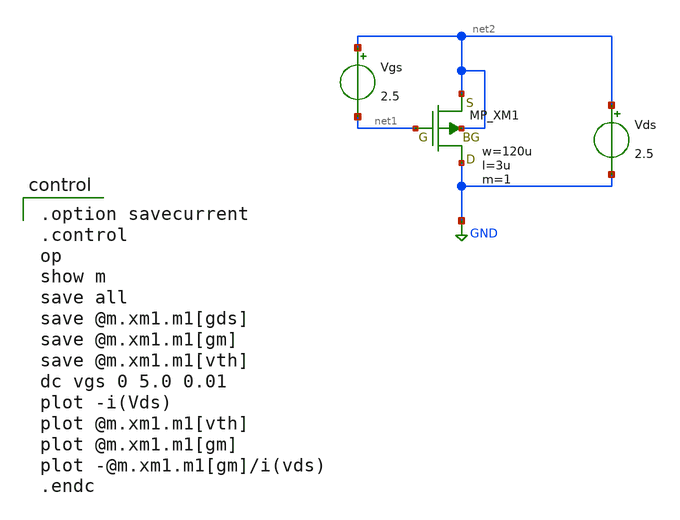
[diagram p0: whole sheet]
** sch_path: member_project/OPAMP/ShuntaroOhno/xschem/pmos_id_vgs.sch
**.subckt pmos_id_vgs
Vgs net2 net1 2.5
Vds net2 GND 2.5
XM1 GND net1 net2 net2 PMOS w=120u l=3u as=0 ad=0 ps=0 pd=0 nrd=0 nrs=0 m=1
**** begin user architecture code
 .include $::LIB/../ip62_models

.option savecurrent
.control
op
show m
save all
save @m.xm1.m1[gds]
save @m.xm1.m1[gm]
save @m.xm1.m1[vth]
dc vgs 0 5.0 0.01
plot -i(Vds)
plot @m.xm1.m1[vth]
plot @m.xm1.m1[gm]
plot -@m.xm1.m1[gm]/i(vds)
.endc

**** end user architecture code
**.ends
.GLOBAL GND
.end
